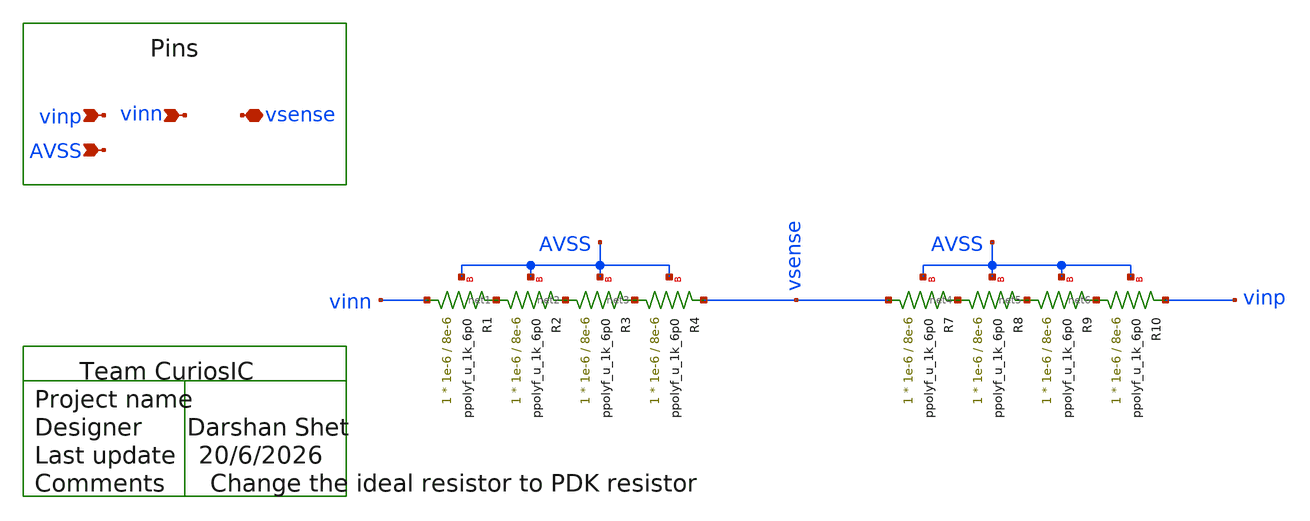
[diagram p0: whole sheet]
** sch_path: design/schematics/CCIA/Instrumentation Amplifier/DS_cic_bms_CMFB_res_div.sch
**.subckt DS_cic_bms_CMFB_res_div vinp vinn vsense AVSS
*.ipin vinp
*.ipin vinn
*.iopin vsense
*.ipin AVSS
XR1 vinn net1 AVSS ppolyf_u_1k_6p0 r_width=1e-6 r_length=8e-6 m=1
XR2 net1 net2 AVSS ppolyf_u_1k_6p0 r_width=1e-6 r_length=8e-6 m=1
XR3 net2 net3 AVSS ppolyf_u_1k_6p0 r_width=1e-6 r_length=8e-6 m=1
XR4 net3 vsense AVSS ppolyf_u_1k_6p0 r_width=1e-6 r_length=8e-6 m=1
XR7 vsense net4 AVSS ppolyf_u_1k_6p0 r_width=1e-6 r_length=8e-6 m=1
XR8 net4 net5 AVSS ppolyf_u_1k_6p0 r_width=1e-6 r_length=8e-6 m=1
XR9 net5 net6 AVSS ppolyf_u_1k_6p0 r_width=1e-6 r_length=8e-6 m=1
XR10 net6 vinp AVSS ppolyf_u_1k_6p0 r_width=1e-6 r_length=8e-6 m=1
**.ends
.end
